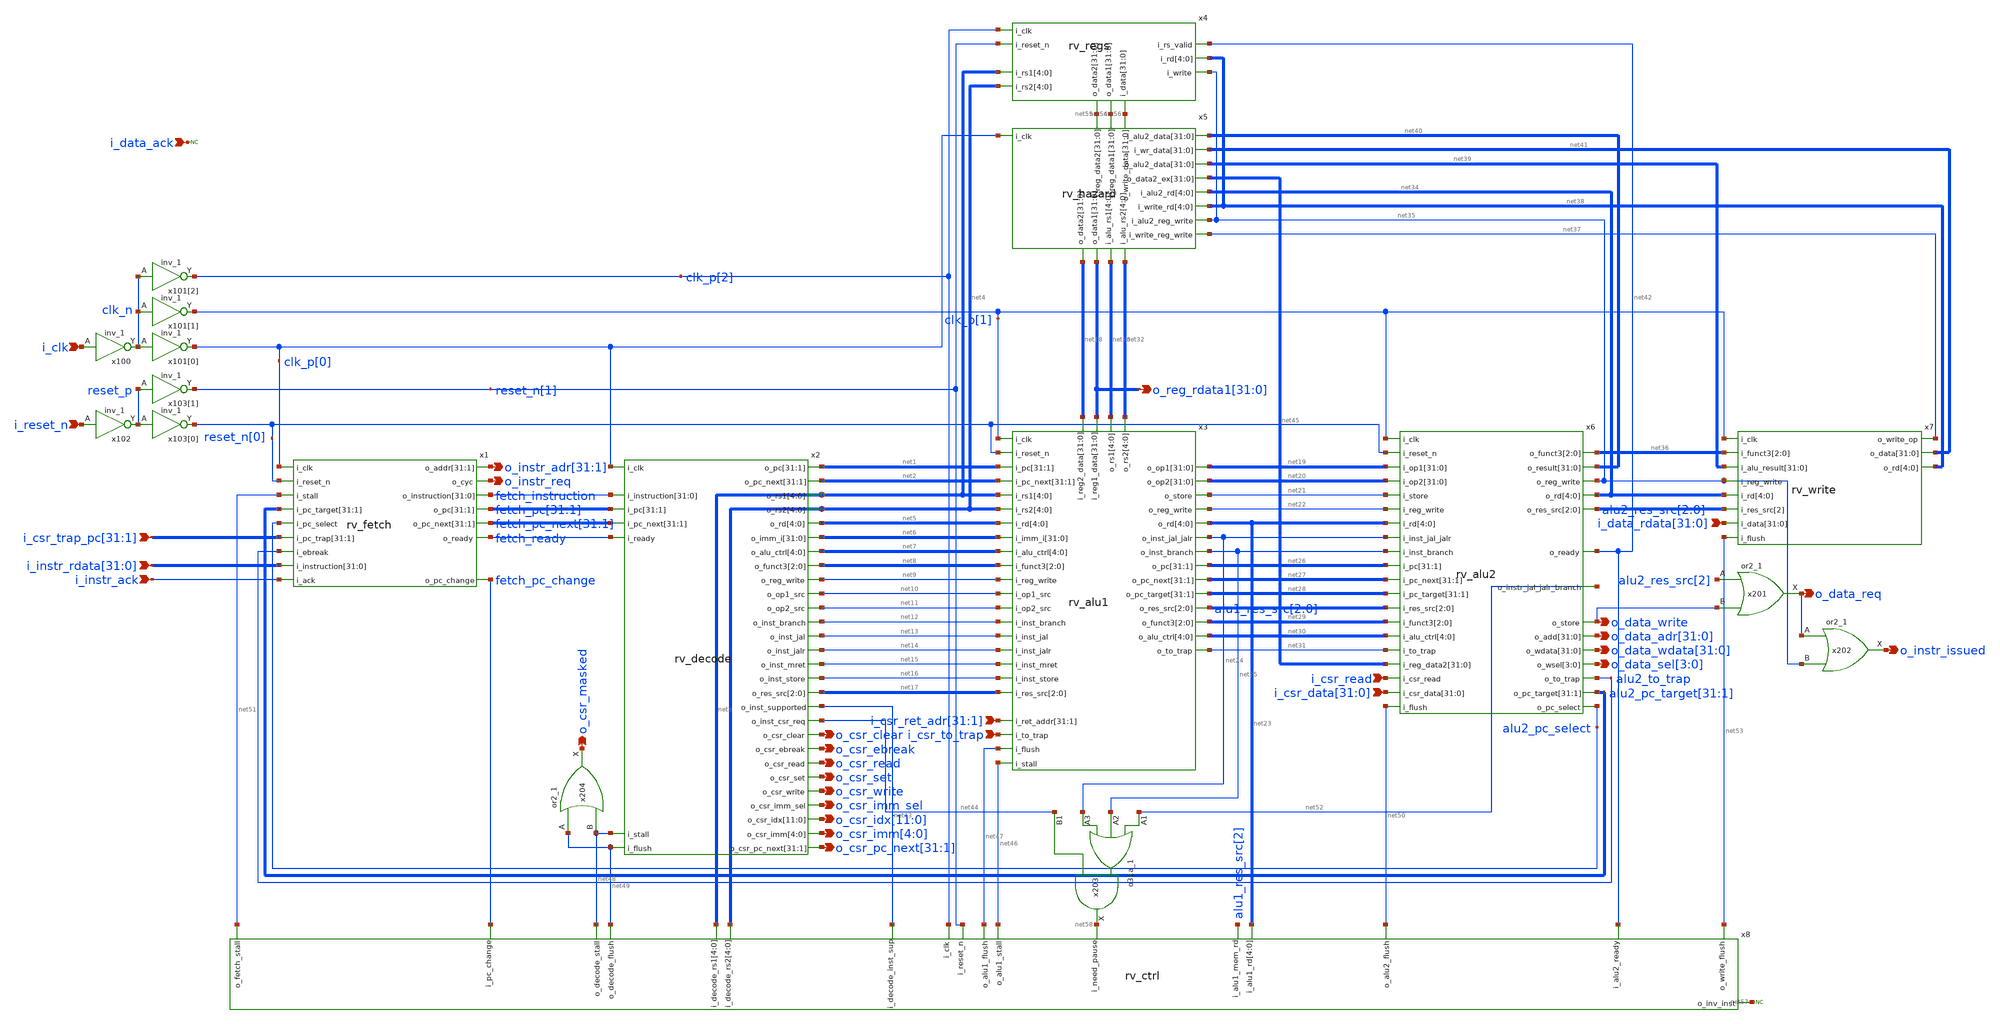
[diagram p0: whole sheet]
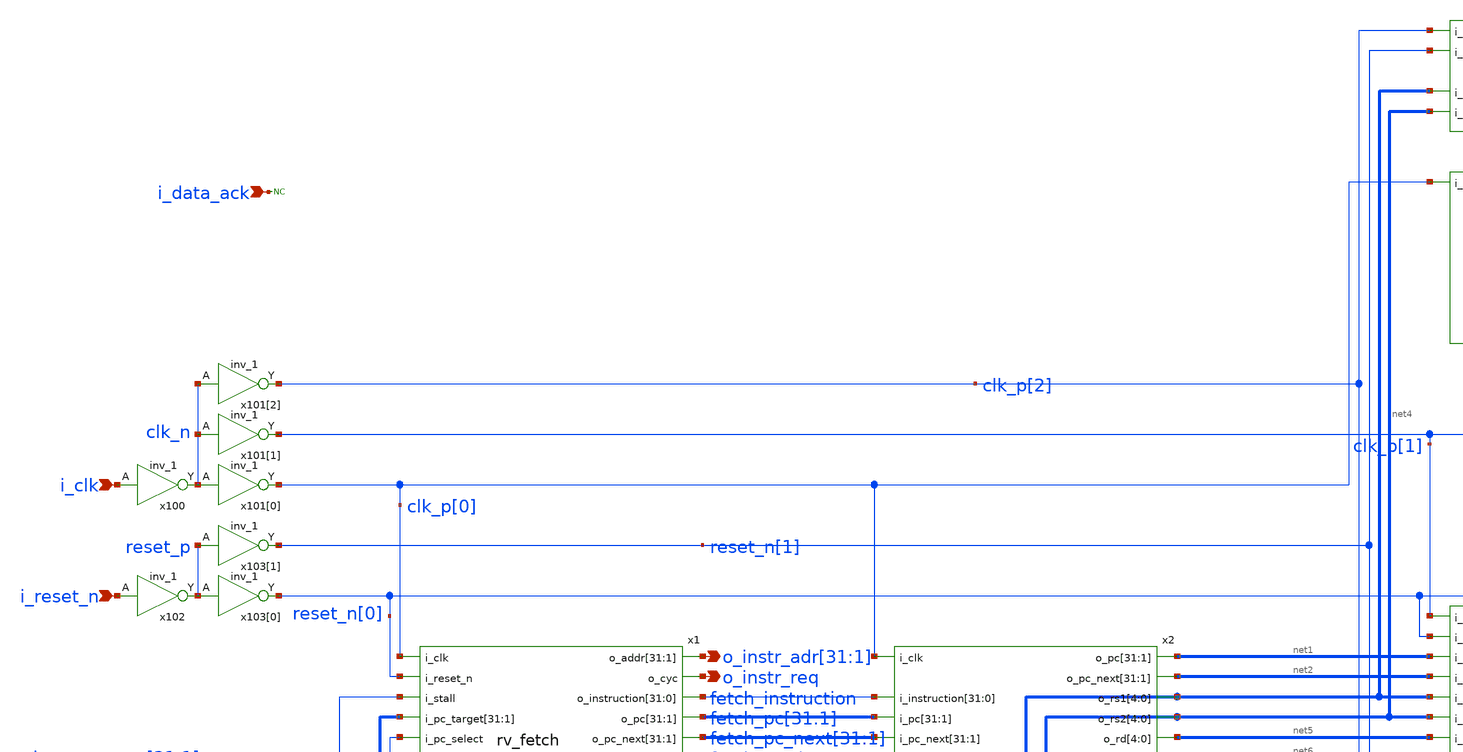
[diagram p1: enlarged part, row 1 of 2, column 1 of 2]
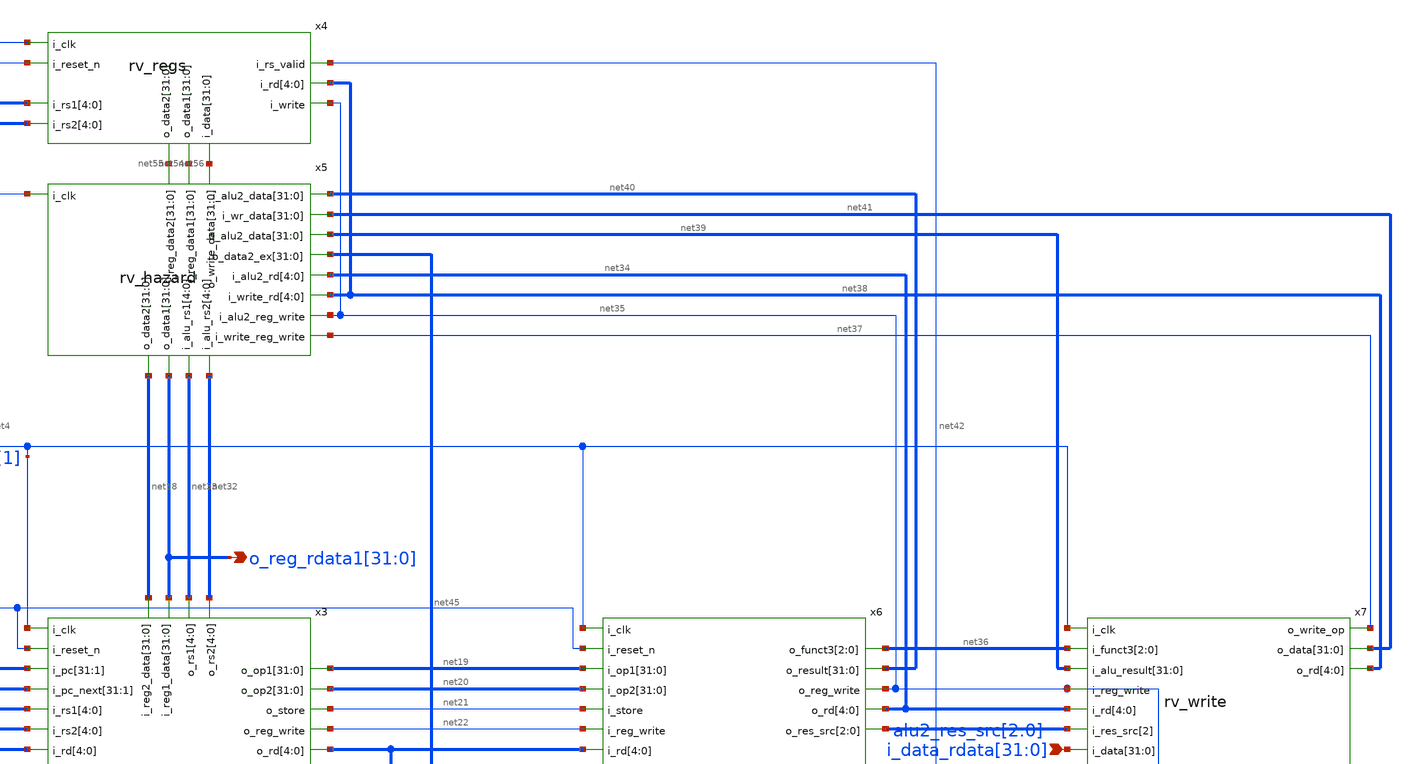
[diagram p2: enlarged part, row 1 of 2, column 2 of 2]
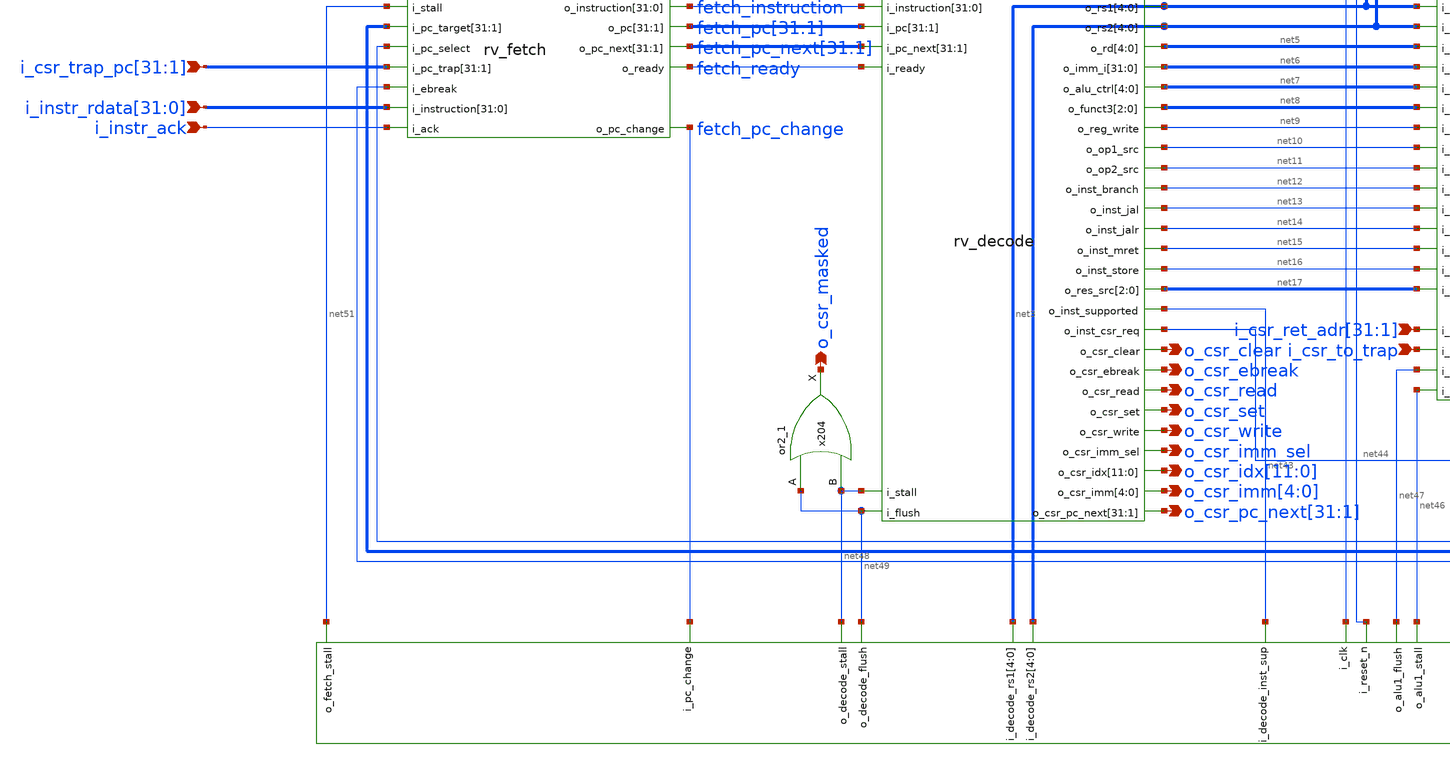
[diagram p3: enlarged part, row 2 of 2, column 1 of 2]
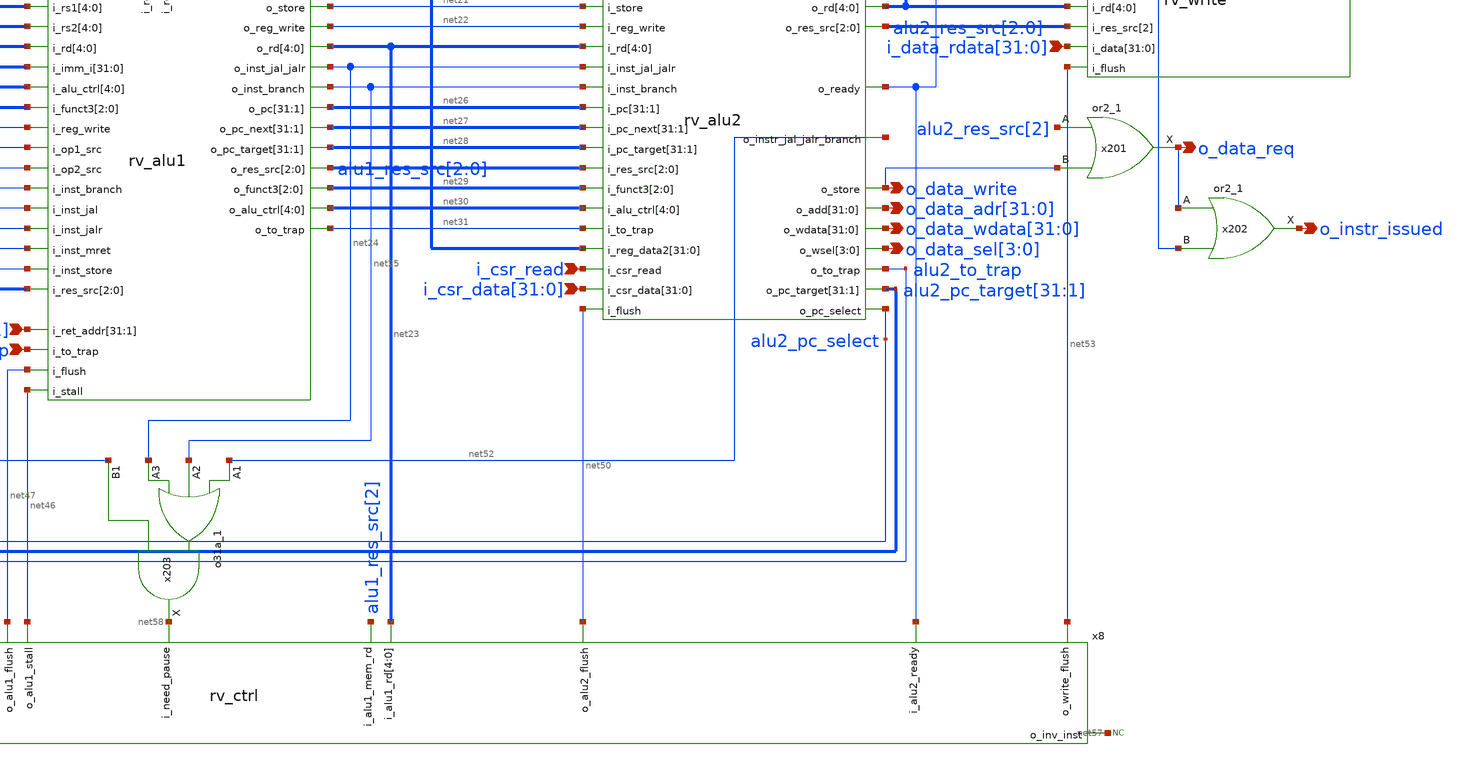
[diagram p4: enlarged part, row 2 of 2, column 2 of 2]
** sch_path: blocks/rv_core/rv_core.sch
**.subckt rv_core i_clk i_reset_n i_csr_read o_csr_clear o_data_req
*+ o_data_wdata[31],o_data_wdata[30],o_data_wdata[29],o_data_wdata[28],o_data_wdata[27],o_data_wdata[26],o_data_wdata[25],o_data_wdata[24],o_data_wdata[23],o_data_wdata[22],o_data_wdata[21],o_data_wdata[20],o_data_wdata[19],o_data_wdata[18],o_data_wdata[17],o_data_wdata[16],o_data_wdata[15],o_data_wdata[14],o_data_wdata[13],o_data_wdata[12],o_data_wdata[11],o_data_wdata[10],o_data_wdata[9],o_data_wdata[8],o_data_wdata[7],o_data_wdata[6],o_data_wdata[5],o_data_wdata[4],o_data_wdata[3],o_data_wdata[2],o_data_wdata[1],o_data_wdata[0] o_instr_issued
*+ o_data_adr[31],o_data_adr[30],o_data_adr[29],o_data_adr[28],o_data_adr[27],o_data_adr[26],o_data_adr[25],o_data_adr[24],o_data_adr[23],o_data_adr[22],o_data_adr[21],o_data_adr[20],o_data_adr[19],o_data_adr[18],o_data_adr[17],o_data_adr[16],o_data_adr[15],o_data_adr[14],o_data_adr[13],o_data_adr[12],o_data_adr[11],o_data_adr[10],o_data_adr[9],o_data_adr[8],o_data_adr[7],o_data_adr[6],o_data_adr[5],o_data_adr[4],o_data_adr[3],o_data_adr[2],o_data_adr[1],o_data_adr[0] o_data_sel[3],o_data_sel[2],o_data_sel[1],o_data_sel[0]
*+ i_csr_data[31],i_csr_data[30],i_csr_data[29],i_csr_data[28],i_csr_data[27],i_csr_data[26],i_csr_data[25],i_csr_data[24],i_csr_data[23],i_csr_data[22],i_csr_data[21],i_csr_data[20],i_csr_data[19],i_csr_data[18],i_csr_data[17],i_csr_data[16],i_csr_data[15],i_csr_data[14],i_csr_data[13],i_csr_data[12],i_csr_data[11],i_csr_data[10],i_csr_data[9],i_csr_data[8],i_csr_data[7],i_csr_data[6],i_csr_data[5],i_csr_data[4],i_csr_data[3],i_csr_data[2],i_csr_data[1],i_csr_data[0] i_csr_to_trap o_csr_ebreak o_csr_read o_csr_set o_csr_write o_csr_imm_sel
*+ i_csr_ret_adr[31],i_csr_ret_adr[30],i_csr_ret_adr[29],i_csr_ret_adr[28],i_csr_ret_adr[27],i_csr_ret_adr[26],i_csr_ret_adr[25],i_csr_ret_adr[24],i_csr_ret_adr[23],i_csr_ret_adr[22],i_csr_ret_adr[21],i_csr_ret_adr[20],i_csr_ret_adr[19],i_csr_ret_adr[18],i_csr_ret_adr[17],i_csr_ret_adr[16],i_csr_ret_adr[15],i_csr_ret_adr[14],i_csr_ret_adr[13],i_csr_ret_adr[12],i_csr_ret_adr[11],i_csr_ret_adr[10],i_csr_ret_adr[9],i_csr_ret_adr[8],i_csr_ret_adr[7],i_csr_ret_adr[6],i_csr_ret_adr[5],i_csr_ret_adr[4],i_csr_ret_adr[3],i_csr_ret_adr[2],i_csr_ret_adr[1]
*+ i_csr_trap_pc[31],i_csr_trap_pc[30],i_csr_trap_pc[29],i_csr_trap_pc[28],i_csr_trap_pc[27],i_csr_trap_pc[26],i_csr_trap_pc[25],i_csr_trap_pc[24],i_csr_trap_pc[23],i_csr_trap_pc[22],i_csr_trap_pc[21],i_csr_trap_pc[20],i_csr_trap_pc[19],i_csr_trap_pc[18],i_csr_trap_pc[17],i_csr_trap_pc[16],i_csr_trap_pc[15],i_csr_trap_pc[14],i_csr_trap_pc[13],i_csr_trap_pc[12],i_csr_trap_pc[11],i_csr_trap_pc[10],i_csr_trap_pc[9],i_csr_trap_pc[8],i_csr_trap_pc[7],i_csr_trap_pc[6],i_csr_trap_pc[5],i_csr_trap_pc[4],i_csr_trap_pc[3],i_csr_trap_pc[2],i_csr_trap_pc[1]
*+ o_csr_idx[11],o_csr_idx[10],o_csr_idx[9],o_csr_idx[8],o_csr_idx[7],o_csr_idx[6],o_csr_idx[5],o_csr_idx[4],o_csr_idx[3],o_csr_idx[2],o_csr_idx[1],o_csr_idx[0] o_csr_imm[4],o_csr_imm[3],o_csr_imm[2],o_csr_imm[1],o_csr_imm[0]
*+ o_csr_pc_next[31],o_csr_pc_next[30],o_csr_pc_next[29],o_csr_pc_next[28],o_csr_pc_next[27],o_csr_pc_next[26],o_csr_pc_next[25],o_csr_pc_next[24],o_csr_pc_next[23],o_csr_pc_next[22],o_csr_pc_next[21],o_csr_pc_next[20],o_csr_pc_next[19],o_csr_pc_next[18],o_csr_pc_next[17],o_csr_pc_next[16],o_csr_pc_next[15],o_csr_pc_next[14],o_csr_pc_next[13],o_csr_pc_next[12],o_csr_pc_next[11],o_csr_pc_next[10],o_csr_pc_next[9],o_csr_pc_next[8],o_csr_pc_next[7],o_csr_pc_next[6],o_csr_pc_next[5],o_csr_pc_next[4],o_csr_pc_next[3],o_csr_pc_next[2],o_csr_pc_next[1]
*+ o_reg_rdata1[31],o_reg_rdata1[30],o_reg_rdata1[29],o_reg_rdata1[28],o_reg_rdata1[27],o_reg_rdata1[26],o_reg_rdata1[25],o_reg_rdata1[24],o_reg_rdata1[23],o_reg_rdata1[22],o_reg_rdata1[21],o_reg_rdata1[20],o_reg_rdata1[19],o_reg_rdata1[18],o_reg_rdata1[17],o_reg_rdata1[16],o_reg_rdata1[15],o_reg_rdata1[14],o_reg_rdata1[13],o_reg_rdata1[12],o_reg_rdata1[11],o_reg_rdata1[10],o_reg_rdata1[9],o_reg_rdata1[8],o_reg_rdata1[7],o_reg_rdata1[6],o_reg_rdata1[5],o_reg_rdata1[4],o_reg_rdata1[3],o_reg_rdata1[2],o_reg_rdata1[1],o_reg_rdata1[0] i_data_ack o_data_write
*+ i_data_rdata[31],i_data_rdata[30],i_data_rdata[29],i_data_rdata[28],i_data_rdata[27],i_data_rdata[26],i_data_rdata[25],i_data_rdata[24],i_data_rdata[23],i_data_rdata[22],i_data_rdata[21],i_data_rdata[20],i_data_rdata[19],i_data_rdata[18],i_data_rdata[17],i_data_rdata[16],i_data_rdata[15],i_data_rdata[14],i_data_rdata[13],i_data_rdata[12],i_data_rdata[11],i_data_rdata[10],i_data_rdata[9],i_data_rdata[8],i_data_rdata[7],i_data_rdata[6],i_data_rdata[5],i_data_rdata[4],i_data_rdata[3],i_data_rdata[2],i_data_rdata[1],i_data_rdata[0] i_instr_ack o_instr_req
*+ i_instr_rdata[31],i_instr_rdata[30],i_instr_rdata[29],i_instr_rdata[28],i_instr_rdata[27],i_instr_rdata[26],i_instr_rdata[25],i_instr_rdata[24],i_instr_rdata[23],i_instr_rdata[22],i_instr_rdata[21],i_instr_rdata[20],i_instr_rdata[19],i_instr_rdata[18],i_instr_rdata[17],i_instr_rdata[16],i_instr_rdata[15],i_instr_rdata[14],i_instr_rdata[13],i_instr_rdata[12],i_instr_rdata[11],i_instr_rdata[10],i_instr_rdata[9],i_instr_rdata[8],i_instr_rdata[7],i_instr_rdata[6],i_instr_rdata[5],i_instr_rdata[4],i_instr_rdata[3],i_instr_rdata[2],i_instr_rdata[1],i_instr_rdata[0]
*+ o_instr_adr[31],o_instr_adr[30],o_instr_adr[29],o_instr_adr[28],o_instr_adr[27],o_instr_adr[26],o_instr_adr[25],o_instr_adr[24],o_instr_adr[23],o_instr_adr[22],o_instr_adr[21],o_instr_adr[20],o_instr_adr[19],o_instr_adr[18],o_instr_adr[17],o_instr_adr[16],o_instr_adr[15],o_instr_adr[14],o_instr_adr[13],o_instr_adr[12],o_instr_adr[11],o_instr_adr[10],o_instr_adr[9],o_instr_adr[8],o_instr_adr[7],o_instr_adr[6],o_instr_adr[5],o_instr_adr[4],o_instr_adr[3],o_instr_adr[2],o_instr_adr[1] o_csr_masked
*.ipin i_clk
*.ipin i_reset_n
*.ipin i_csr_read
*.opin o_csr_clear
*.opin o_data_req
*.opin
*+ o_data_wdata[31],o_data_wdata[30],o_data_wdata[29],o_data_wdata[28],o_data_wdata[27],o_data_wdata[26],o_data_wdata[25],o_data_wdata[24],o_data_wdata[23],o_data_wdata[22],o_data_wdata[21],o_data_wdata[20],o_data_wdata[19],o_data_wdata[18],o_data_wdata[17],o_data_wdata[16],o_data_wdata[15],o_data_wdata[14],o_data_wdata[13],o_data_wdata[12],o_data_wdata[11],o_data_wdata[10],o_data_wdata[9],o_data_wdata[8],o_data_wdata[7],o_data_wdata[6],o_data_wdata[5],o_data_wdata[4],o_data_wdata[3],o_data_wdata[2],o_data_wdata[1],o_data_wdata[0]
*.opin o_instr_issued
*.opin
*+ o_data_adr[31],o_data_adr[30],o_data_adr[29],o_data_adr[28],o_data_adr[27],o_data_adr[26],o_data_adr[25],o_data_adr[24],o_data_adr[23],o_data_adr[22],o_data_adr[21],o_data_adr[20],o_data_adr[19],o_data_adr[18],o_data_adr[17],o_data_adr[16],o_data_adr[15],o_data_adr[14],o_data_adr[13],o_data_adr[12],o_data_adr[11],o_data_adr[10],o_data_adr[9],o_data_adr[8],o_data_adr[7],o_data_adr[6],o_data_adr[5],o_data_adr[4],o_data_adr[3],o_data_adr[2],o_data_adr[1],o_data_adr[0]
*.opin o_data_sel[3],o_data_sel[2],o_data_sel[1],o_data_sel[0]
*.ipin
*+ i_csr_data[31],i_csr_data[30],i_csr_data[29],i_csr_data[28],i_csr_data[27],i_csr_data[26],i_csr_data[25],i_csr_data[24],i_csr_data[23],i_csr_data[22],i_csr_data[21],i_csr_data[20],i_csr_data[19],i_csr_data[18],i_csr_data[17],i_csr_data[16],i_csr_data[15],i_csr_data[14],i_csr_data[13],i_csr_data[12],i_csr_data[11],i_csr_data[10],i_csr_data[9],i_csr_data[8],i_csr_data[7],i_csr_data[6],i_csr_data[5],i_csr_data[4],i_csr_data[3],i_csr_data[2],i_csr_data[1],i_csr_data[0]
*.ipin i_csr_to_trap
*.opin o_csr_ebreak
*.opin o_csr_read
*.opin o_csr_set
*.opin o_csr_write
*.opin o_csr_imm_sel
*.ipin
*+ i_csr_ret_adr[31],i_csr_ret_adr[30],i_csr_ret_adr[29],i_csr_ret_adr[28],i_csr_ret_adr[27],i_csr_ret_adr[26],i_csr_ret_adr[25],i_csr_ret_adr[24],i_csr_ret_adr[23],i_csr_ret_adr[22],i_csr_ret_adr[21],i_csr_ret_adr[20],i_csr_ret_adr[19],i_csr_ret_adr[18],i_csr_ret_adr[17],i_csr_ret_adr[16],i_csr_ret_adr[15],i_csr_ret_adr[14],i_csr_ret_adr[13],i_csr_ret_adr[12],i_csr_ret_adr[11],i_csr_ret_adr[10],i_csr_ret_adr[9],i_csr_ret_adr[8],i_csr_ret_adr[7],i_csr_ret_adr[6],i_csr_ret_adr[5],i_csr_ret_adr[4],i_csr_ret_adr[3],i_csr_ret_adr[2],i_csr_ret_adr[1]
*.ipin
*+ i_csr_trap_pc[31],i_csr_trap_pc[30],i_csr_trap_pc[29],i_csr_trap_pc[28],i_csr_trap_pc[27],i_csr_trap_pc[26],i_csr_trap_pc[25],i_csr_trap_pc[24],i_csr_trap_pc[23],i_csr_trap_pc[22],i_csr_trap_pc[21],i_csr_trap_pc[20],i_csr_trap_pc[19],i_csr_trap_pc[18],i_csr_trap_pc[17],i_csr_trap_pc[16],i_csr_trap_pc[15],i_csr_trap_pc[14],i_csr_trap_pc[13],i_csr_trap_pc[12],i_csr_trap_pc[11],i_csr_trap_pc[10],i_csr_trap_pc[9],i_csr_trap_pc[8],i_csr_trap_pc[7],i_csr_trap_pc[6],i_csr_trap_pc[5],i_csr_trap_pc[4],i_csr_trap_pc[3],i_csr_trap_pc[2],i_csr_trap_pc[1]
*.opin
*+ o_csr_idx[11],o_csr_idx[10],o_csr_idx[9],o_csr_idx[8],o_csr_idx[7],o_csr_idx[6],o_csr_idx[5],o_csr_idx[4],o_csr_idx[3],o_csr_idx[2],o_csr_idx[1],o_csr_idx[0]
*.opin o_csr_imm[4],o_csr_imm[3],o_csr_imm[2],o_csr_imm[1],o_csr_imm[0]
*.opin
*+ o_csr_pc_next[31],o_csr_pc_next[30],o_csr_pc_next[29],o_csr_pc_next[28],o_csr_pc_next[27],o_csr_pc_next[26],o_csr_pc_next[25],o_csr_pc_next[24],o_csr_pc_next[23],o_csr_pc_next[22],o_csr_pc_next[21],o_csr_pc_next[20],o_csr_pc_next[19],o_csr_pc_next[18],o_csr_pc_next[17],o_csr_pc_next[16],o_csr_pc_next[15],o_csr_pc_next[14],o_csr_pc_next[13],o_csr_pc_next[12],o_csr_pc_next[11],o_csr_pc_next[10],o_csr_pc_next[9],o_csr_pc_next[8],o_csr_pc_next[7],o_csr_pc_next[6],o_csr_pc_next[5],o_csr_pc_next[4],o_csr_pc_next[3],o_csr_pc_next[2],o_csr_pc_next[1]
*.opin
*+ o_reg_rdata1[31],o_reg_rdata1[30],o_reg_rdata1[29],o_reg_rdata1[28],o_reg_rdata1[27],o_reg_rdata1[26],o_reg_rdata1[25],o_reg_rdata1[24],o_reg_rdata1[23],o_reg_rdata1[22],o_reg_rdata1[21],o_reg_rdata1[20],o_reg_rdata1[19],o_reg_rdata1[18],o_reg_rdata1[17],o_reg_rdata1[16],o_reg_rdata1[15],o_reg_rdata1[14],o_reg_rdata1[13],o_reg_rdata1[12],o_reg_rdata1[11],o_reg_rdata1[10],o_reg_rdata1[9],o_reg_rdata1[8],o_reg_rdata1[7],o_reg_rdata1[6],o_reg_rdata1[5],o_reg_rdata1[4],o_reg_rdata1[3],o_reg_rdata1[2],o_reg_rdata1[1],o_reg_rdata1[0]
*.ipin i_data_ack
*.opin o_data_write
*.ipin
*+ i_data_rdata[31],i_data_rdata[30],i_data_rdata[29],i_data_rdata[28],i_data_rdata[27],i_data_rdata[26],i_data_rdata[25],i_data_rdata[24],i_data_rdata[23],i_data_rdata[22],i_data_rdata[21],i_data_rdata[20],i_data_rdata[19],i_data_rdata[18],i_data_rdata[17],i_data_rdata[16],i_data_rdata[15],i_data_rdata[14],i_data_rdata[13],i_data_rdata[12],i_data_rdata[11],i_data_rdata[10],i_data_rdata[9],i_data_rdata[8],i_data_rdata[7],i_data_rdata[6],i_data_rdata[5],i_data_rdata[4],i_data_rdata[3],i_data_rdata[2],i_data_rdata[1],i_data_rdata[0]
*.ipin i_instr_ack
*.opin o_instr_req
*.ipin
*+ i_instr_rdata[31],i_instr_rdata[30],i_instr_rdata[29],i_instr_rdata[28],i_instr_rdata[27],i_instr_rdata[26],i_instr_rdata[25],i_instr_rdata[24],i_instr_rdata[23],i_instr_rdata[22],i_instr_rdata[21],i_instr_rdata[20],i_instr_rdata[19],i_instr_rdata[18],i_instr_rdata[17],i_instr_rdata[16],i_instr_rdata[15],i_instr_rdata[14],i_instr_rdata[13],i_instr_rdata[12],i_instr_rdata[11],i_instr_rdata[10],i_instr_rdata[9],i_instr_rdata[8],i_instr_rdata[7],i_instr_rdata[6],i_instr_rdata[5],i_instr_rdata[4],i_instr_rdata[3],i_instr_rdata[2],i_instr_rdata[1],i_instr_rdata[0]
*.opin
*+ o_instr_adr[31],o_instr_adr[30],o_instr_adr[29],o_instr_adr[28],o_instr_adr[27],o_instr_adr[26],o_instr_adr[25],o_instr_adr[24],o_instr_adr[23],o_instr_adr[22],o_instr_adr[21],o_instr_adr[20],o_instr_adr[19],o_instr_adr[18],o_instr_adr[17],o_instr_adr[16],o_instr_adr[15],o_instr_adr[14],o_instr_adr[13],o_instr_adr[12],o_instr_adr[11],o_instr_adr[10],o_instr_adr[9],o_instr_adr[8],o_instr_adr[7],o_instr_adr[6],o_instr_adr[5],o_instr_adr[4],o_instr_adr[3],o_instr_adr[2],o_instr_adr[1]
*.opin o_csr_masked
x1 fetch_pc_change clk_p[0] reset_n[0] o_instr_adr[31] o_instr_adr[30] o_instr_adr[29]
+ o_instr_adr[28] o_instr_adr[27] o_instr_adr[26] o_instr_adr[25] o_instr_adr[24] o_instr_adr[23] o_instr_adr[22]
+ o_instr_adr[21] o_instr_adr[20] o_instr_adr[19] o_instr_adr[18] o_instr_adr[17] o_instr_adr[16] o_instr_adr[15]
+ o_instr_adr[14] o_instr_adr[13] o_instr_adr[12] o_instr_adr[11] o_instr_adr[10] o_instr_adr[9] o_instr_adr[8]
+ o_instr_adr[7] o_instr_adr[6] o_instr_adr[5] o_instr_adr[4] o_instr_adr[3] o_instr_adr[2] o_instr_adr[1]
+ o_instr_req net51 fetch_instruction fetch_instruction fetch_instruction fetch_instruction fetch_instruction
+ fetch_instruction fetch_instruction fetch_instruction fetch_instruction fetch_instruction fetch_instruction
+ fetch_instruction fetch_instruction fetch_instruction fetch_instruction fetch_instruction fetch_instruction
+ fetch_instruction fetch_instruction fetch_instruction fetch_instruction fetch_instruction fetch_instruction
+ fetch_instruction fetch_instruction fetch_instruction fetch_instruction fetch_instruction fetch_instruction
+ fetch_instruction fetch_instruction fetch_instruction alu2_pc_target[31] alu2_pc_target[30] alu2_pc_target[29]
+ alu2_pc_target[28] alu2_pc_target[27] alu2_pc_target[26] alu2_pc_target[25] alu2_pc_target[24] alu2_pc_target[23]
+ alu2_pc_target[22] alu2_pc_target[21] alu2_pc_target[20] alu2_pc_target[19] alu2_pc_target[18] alu2_pc_target[17]
+ alu2_pc_target[16] alu2_pc_target[15] alu2_pc_target[14] alu2_pc_target[13] alu2_pc_target[12] alu2_pc_target[11]
+ alu2_pc_target[10] alu2_pc_target[9] alu2_pc_target[8] alu2_pc_target[7] alu2_pc_target[6] alu2_pc_target[5]
+ alu2_pc_target[4] alu2_pc_target[3] alu2_pc_target[2] alu2_pc_target[1] alu2_pc_select fetch_pc[31] fetch_pc[30]
+ fetch_pc[29] fetch_pc[28] fetch_pc[27] fetch_pc[26] fetch_pc[25] fetch_pc[24] fetch_pc[23] fetch_pc[22]
+ fetch_pc[21] fetch_pc[20] fetch_pc[19] fetch_pc[18] fetch_pc[17] fetch_pc[16] fetch_pc[15] fetch_pc[14]
+ fetch_pc[13] fetch_pc[12] fetch_pc[11] fetch_pc[10] fetch_pc[9] fetch_pc[8] fetch_pc[7] fetch_pc[6] fetch_pc[5]
+ fetch_pc[4] fetch_pc[3] fetch_pc[2] fetch_pc[1] fetch_pc_next[31] fetch_pc_next[30] fetch_pc_next[29]
+ fetch_pc_next[28] fetch_pc_next[27] fetch_pc_next[26] fetch_pc_next[25] fetch_pc_next[24] fetch_pc_next[23]
+ fetch_pc_next[22] fetch_pc_next[21] fetch_pc_next[20] fetch_pc_next[19] fetch_pc_next[18] fetch_pc_next[17]
+ fetch_pc_next[16] fetch_pc_next[15] fetch_pc_next[14] fetch_pc_next[13] fetch_pc_next[12] fetch_pc_next[11]
+ fetch_pc_next[10] fetch_pc_next[9] fetch_pc_next[8] fetch_pc_next[7] fetch_pc_next[6] fetch_pc_next[5]
+ fetch_pc_next[4] fetch_pc_next[3] fetch_pc_next[2] fetch_pc_next[1] i_csr_trap_pc[31] i_csr_trap_pc[30]
+ i_csr_trap_pc[29] i_csr_trap_pc[28] i_csr_trap_pc[27] i_csr_trap_pc[26] i_csr_trap_pc[25] i_csr_trap_pc[24]
+ i_csr_trap_pc[23] i_csr_trap_pc[22] i_csr_trap_pc[21] i_csr_trap_pc[20] i_csr_trap_pc[19] i_csr_trap_pc[18]
+ i_csr_trap_pc[17] i_csr_trap_pc[16] i_csr_trap_pc[15] i_csr_trap_pc[14] i_csr_trap_pc[13] i_csr_trap_pc[12]
+ i_csr_trap_pc[11] i_csr_trap_pc[10] i_csr_trap_pc[9] i_csr_trap_pc[8] i_csr_trap_pc[7] i_csr_trap_pc[6]
+ i_csr_trap_pc[5] i_csr_trap_pc[4] i_csr_trap_pc[3] i_csr_trap_pc[2] i_csr_trap_pc[1] fetch_ready alu2_to_trap
+ i_instr_rdata[31] i_instr_rdata[30] i_instr_rdata[29] i_instr_rdata[28] i_instr_rdata[27] i_instr_rdata[26]
+ i_instr_rdata[25] i_instr_rdata[24] i_instr_rdata[23] i_instr_rdata[22] i_instr_rdata[21] i_instr_rdata[20]
+ i_instr_rdata[19] i_instr_rdata[18] i_instr_rdata[17] i_instr_rdata[16] i_instr_rdata[15] i_instr_rdata[14]
+ i_instr_rdata[13] i_instr_rdata[12] i_instr_rdata[11] i_instr_rdata[10] i_instr_rdata[9] i_instr_rdata[8]
+ i_instr_rdata[7] i_instr_rdata[6] i_instr_rdata[5] i_instr_rdata[4] i_instr_rdata[3] i_instr_rdata[2]
+ i_instr_rdata[1] i_instr_rdata[0] i_instr_ack rv_fetch
x100 i_clk VSS VSS VCC VCC clk_n sky130_fd_sc_hs__inv_1
x102 i_reset_n VSS VSS VCC VCC reset_p sky130_fd_sc_hs__inv_1
x103[0] reset_p VSS VSS VCC VCC reset_n[0] sky130_fd_sc_hs__inv_1
x101[2] clk_n VSS VSS VCC VCC clk_p[2] sky130_fd_sc_hs__inv_1
x101[1] clk_n VSS VSS VCC VCC clk_p[1] sky130_fd_sc_hs__inv_1
x101[0] clk_n VSS VSS VCC VCC clk_p[0] sky130_fd_sc_hs__inv_1
x103[1] reset_p VSS VSS VCC VCC reset_n[1] sky130_fd_sc_hs__inv_1
x2 net1[30] net1[29] net1[28] net1[27] net1[26] net1[25] net1[24] net1[23] net1[22] net1[21]
+ net1[20] net1[19] net1[18] net1[17] net1[16] net1[15] net1[14] net1[13] net1[12] net1[11] net1[10] net1[9]
+ net1[8] net1[7] net1[6] net1[5] net1[4] net1[3] net1[2] net1[1] net1[0] clk_p[0] net48 net2[30] net2[29]
+ net2[28] net2[27] net2[26] net2[25] net2[24] net2[23] net2[22] net2[21] net2[20] net2[19] net2[18] net2[17]
+ net2[16] net2[15] net2[14] net2[13] net2[12] net2[11] net2[10] net2[9] net2[8] net2[7] net2[6] net2[5]
+ net2[4] net2[3] net2[2] net2[1] net2[0] net49 net3[4] net3[3] net3[2] net3[1] net3[0] fetch_instruction
+ fetch_instruction fetch_instruction fetch_instruction fetch_instruction fetch_instruction fetch_instruction
+ fetch_instruction fetch_instruction fetch_instruction fetch_instruction fetch_instruction fetch_instruction
+ fetch_instruction fetch_instruction fetch_instruction fetch_instruction fetch_instruction fetch_instruction
+ fetch_instruction fetch_instruction fetch_instruction fetch_instruction fetch_instruction fetch_instruction
+ fetch_instruction fetch_instruction fetch_instruction fetch_instruction fetch_instruction fetch_instruction
+ fetch_instruction net4[4] net4[3] net4[2] net4[1] net4[0] net5[4] net5[3] net5[2] net5[1] net5[0] fetch_pc[31]
+ fetch_pc[30] fetch_pc[29] fetch_pc[28] fetch_pc[27] fetch_pc[26] fetch_pc[25] fetch_pc[24] fetch_pc[23]
+ fetch_pc[22] fetch_pc[21] fetch_pc[20] fetch_pc[19] fetch_pc[18] fetch_pc[17] fetch_pc[16] fetch_pc[15]
+ fetch_pc[14] fetch_pc[13] fetch_pc[12] fetch_pc[11] fetch_pc[10] fetch_pc[9] fetch_pc[8] fetch_pc[7] fetch_pc[6]
+ fetch_pc[5] fetch_pc[4] fetch_pc[3] fetch_pc[2] fetch_pc[1] net6[31] net6[30] net6[29] net6[28] net6[27]
+ net6[26] net6[25] net6[24] net6[23] net6[22] net6[21] net6[20] net6[19] net6[18] net6[17] net6[16] net6[15]
+ net6[14] net6[13] net6[12] net6[11] net6[10] net6[9] net6[8] net6[7] net6[6] net6[5] net6[4] net6[3] net6[2]
+ net6[1] net6[0] fetch_pc_next[31] fetch_pc_next[30] fetch_pc_next[29] fetch_pc_next[28] fetch_pc_next[27]
+ fetch_pc_next[26] fetch_pc_next[25] fetch_pc_next[24] fetch_pc_next[23] fetch_pc_next[22] fetch_pc_next[21]
+ fetch_pc_next[20] fetch_pc_next[19] fetch_pc_next[18] fetch_pc_next[17] fetch_pc_next[16] fetch_pc_next[15]
+ fetch_pc_next[14] fetch_pc_next[13] fetch_pc_next[12] fetch_pc_next[11] fetch_pc_next[10] fetch_pc_next[9]
+ fetch_pc_next[8] fetch_pc_next[7] fetch_pc_next[6] fetch_pc_next[5] fetch_pc_next[4] fetch_pc_next[3]
+ fetch_pc_next[2] fetch_pc_next[1] fetch_ready net7[4] net7[3] net7[2] net7[1] net7[0] net8[2] net8[1] net8[0] net9
+ net10 net11 net12 net44 net13 net14 net15 net16 net43 net17[2] net17[1] net17[0] o_csr_clear o_csr_ebreak
+ o_csr_read o_csr_set o_csr_write o_csr_imm_sel o_csr_idx[11] o_csr_idx[10] o_csr_idx[9] o_csr_idx[8]
+ o_csr_idx[7] o_csr_idx[6] o_csr_idx[5] o_csr_idx[4] o_csr_idx[3] o_csr_idx[2] o_csr_idx[1] o_csr_idx[0]
+ o_csr_imm[4] o_csr_imm[3] o_csr_imm[2] o_csr_imm[1] o_csr_imm[0] o_csr_pc_next[31] o_csr_pc_next[30]
+ o_csr_pc_next[29] o_csr_pc_next[28] o_csr_pc_next[27] o_csr_pc_next[26] o_csr_pc_next[25] o_csr_pc_next[24]
+ o_csr_pc_next[23] o_csr_pc_next[22] o_csr_pc_next[21] o_csr_pc_next[20] o_csr_pc_next[19] o_csr_pc_next[18]
+ o_csr_pc_next[17] o_csr_pc_next[16] o_csr_pc_next[15] o_csr_pc_next[14] o_csr_pc_next[13] o_csr_pc_next[12]
+ o_csr_pc_next[11] o_csr_pc_next[10] o_csr_pc_next[9] o_csr_pc_next[8] o_csr_pc_next[7] o_csr_pc_next[6]
+ o_csr_pc_next[5] o_csr_pc_next[4] o_csr_pc_next[3] o_csr_pc_next[2] o_csr_pc_next[1] rv_decode
x3 clk_p[1] net19[31] net19[30] net19[29] net19[28] net19[27] net19[26] net19[25] net19[24]
+ net19[23] net19[22] net19[21] net19[20] net19[19] net19[18] net19[17] net19[16] net19[15] net19[14] net19[13]
+ net19[12] net19[11] net19[10] net19[9] net19[8] net19[7] net19[6] net19[5] net19[4] net19[3] net19[2]
+ net19[1] net19[0] reset_n[0] net20[31] net20[30] net20[29] net20[28] net20[27] net20[26] net20[25] net20[24]
+ net20[23] net20[22] net20[21] net20[20] net20[19] net20[18] net20[17] net20[16] net20[15] net20[14] net20[13]
+ net20[12] net20[11] net20[10] net20[9] net20[8] net20[7] net20[6] net20[5] net20[4] net20[3] net20[2]
+ net20[1] net20[0] net1[30] net1[29] net1[28] net1[27] net1[26] net1[25] net1[24] net1[23] net1[22] net1[21]
+ net1[20] net1[19] net1[18] net1[17] net1[16] net1[15] net1[14] net1[13] net1[12] net1[11] net1[10] net1[9]
+ net1[8] net1[7] net1[6] net1[5] net1[4] net1[3] net1[2] net1[1] net1[0] net21 net22 net2[30] net2[29]
+ net2[28] net2[27] net2[26] net2[25] net2[24] net2[23] net2[22] net2[21] net2[20] net2[19] net2[18] net2[17]
+ net2[16] net2[15] net2[14] net2[13] net2[12] net2[11] net2[10] net2[9] net2[8] net2[7] net2[6] net2[5]
+ net2[4] net2[3] net2[2] net2[1] net2[0] net33[4] net33[3] net33[2] net33[1] net33[0] net3[4] net3[3]
+ net3[2] net3[1] net3[0] net4[4] net4[3] net4[2] net4[1] net4[0] net32[4] net32[3] net32[2] net32[1]
+ net32[0] net5[4] net5[3] net5[2] net5[1] net5[0] net23[4] net23[3] net23[2] net23[1] net23[0] net6[31]
+ net6[30] net6[29] net6[28] net6[27] net6[26] net6[25] net6[24] net6[23] net6[22] net6[21] net6[20] net6[19]
+ net6[18] net6[17] net6[16] net6[15] net6[14] net6[13] net6[12] net6[11] net6[10] net6[9] net6[8] net6[7]
+ net6[6] net6[5] net6[4] net6[3] net6[2] net6[1] net6[0] net24 net7[4] net7[3] net7[2] net7[1] net7[0] net25
+ net8[2] net8[1] net8[0] net26[30] net26[29] net26[28] net26[27] net26[26] net26[25] net26[24] net26[23]
+ net26[22] net26[21] net26[20] net26[19] net26[18] net26[17] net26[16] net26[15] net26[14] net26[13] net26[12]
+ net26[11] net26[10] net26[9] net26[8] net26[7] net26[6] net26[5] net26[4] net26[3] net26[2] net26[1] net26[0]
+ net27[30] net27[29] net27[28] net27[27] net27[26] net27[25] net27[24] net27[23] net27[22] net27[21] net27[20]
+ net27[19] net27[18] net27[17] net27[16] net27[15] net27[14] net27[13] net27[12] net27[11] net27[10] net27[9]
+ net27[8] net27[7] net27[6] net27[5] net27[4] net27[3] net27[2] net27[1] net27[0] net9 net28[30] net28[29]
+ net28[28] net28[27] net28[26] net28[25] net28[24] net28[23] net28[22] net28[21] net28[20] net28[19] net28[18]
+ net28[17] net28[16] net28[15] net28[14] net28[13] net28[12] net28[11] net28[10] net28[9] net28[8] net28[7]
+ net28[6] net28[5] net28[4] net28[3] net28[2] net28[1] net28[0] net10 net11 alu1_res_src[2] alu1_res_src[1]
+ alu1_res_src[0] net12 net29[2] net29[1] net29[0] net30[4] net30[3] net30[2] net30[1] net30[0] net13 net31 net14
+ net15 net16 net17[2] net17[1] net17[0] o_reg_rdata1[31] o_reg_rdata1[30] o_reg_rdata1[29]
+ o_reg_rdata1[28] o_reg_rdata1[27] o_reg_rdata1[26] o_reg_rdata1[25] o_reg_rdata1[24] o_reg_rdata1[23]
+ o_reg_rdata1[22] o_reg_rdata1[21] o_reg_rdata1[20] o_reg_rdata1[19] o_reg_rdata1[18] o_reg_rdata1[17]
+ o_reg_rdata1[16] o_reg_rdata1[15] o_reg_rdata1[14] o_reg_rdata1[13] o_reg_rdata1[12] o_reg_rdata1[11]
+ o_reg_rdata1[10] o_reg_rdata1[9] o_reg_rdata1[8] o_reg_rdata1[7] o_reg_rdata1[6] o_reg_rdata1[5] o_reg_rdata1[4]
+ o_reg_rdata1[3] o_reg_rdata1[2] o_reg_rdata1[1] o_reg_rdata1[0] net18[31] net18[30] net18[29] net18[28] net18[27]
+ net18[26] net18[25] net18[24] net18[23] net18[22] net18[21] net18[20] net18[19] net18[18] net18[17] net18[16]
+ net18[15] net18[14] net18[13] net18[12] net18[11] net18[10] net18[9] net18[8] net18[7] net18[6] net18[5]
+ net18[4] net18[3] net18[2] net18[1] net18[0] i_csr_to_trap net47 net46 i_csr_ret_adr[31] i_csr_ret_adr[30]
+ i_csr_ret_adr[29] i_csr_ret_adr[28] i_csr_ret_adr[27] i_csr_ret_adr[26] i_csr_ret_adr[25] i_csr_ret_adr[24]
+ i_csr_ret_adr[23] i_csr_ret_adr[22] i_csr_ret_adr[21] i_csr_ret_adr[20] i_csr_ret_adr[19] i_csr_ret_adr[18]
+ i_csr_ret_adr[17] i_csr_ret_adr[16] i_csr_ret_adr[15] i_csr_ret_adr[14] i_csr_ret_adr[13] i_csr_ret_adr[12]
+ i_csr_ret_adr[11] i_csr_ret_adr[10] i_csr_ret_adr[9] i_csr_ret_adr[8] i_csr_ret_adr[7] i_csr_ret_adr[6]
+ i_csr_ret_adr[5] i_csr_ret_adr[4] i_csr_ret_adr[3] i_csr_ret_adr[2] i_csr_ret_adr[1] rv_alu1
x4 net54[31] net54[30] net54[29] net54[28] net54[27] net54[26] net54[25] net54[24] net54[23]
+ net54[22] net54[21] net54[20] net54[19] net54[18] net54[17] net54[16] net54[15] net54[14] net54[13] net54[12]
+ net54[11] net54[10] net54[9] net54[8] net54[7] net54[6] net54[5] net54[4] net54[3] net54[2] net54[1] net54[0]
+ clk_p[2] reset_n[1] net55[31] net55[30] net55[29] net55[28] net55[27] net55[26] net55[25] net55[24]
+ net55[23] net55[22] net55[21] net55[20] net55[19] net55[18] net55[17] net55[16] net55[15] net55[14] net55[13]
+ net55[12] net55[11] net55[10] net55[9] net55[8] net55[7] net55[6] net55[5] net55[4] net55[3] net55[2]
+ net55[1] net55[0] net42 net35 net3[4] net3[3] net3[2] net3[1] net3[0] net4[4] net4[3] net4[2] net4[1]
+ net4[0] net38[4] net38[3] net38[2] net38[1] net38[0] net56[31] net56[30] net56[29] net56[28] net56[27]
+ net56[26] net56[25] net56[24] net56[23] net56[22] net56[21] net56[20] net56[19] net56[18] net56[17] net56[16]
+ net56[15] net56[14] net56[13] net56[12] net56[11] net56[10] net56[9] net56[8] net56[7] net56[6] net56[5]
+ net56[4] net56[3] net56[2] net56[1] net56[0] rv_regs
x5 clk_p[0] o_reg_rdata1[31] o_reg_rdata1[30] o_reg_rdata1[29] o_reg_rdata1[28] o_reg_rdata1[27]
+ o_reg_rdata1[26] o_reg_rdata1[25] o_reg_rdata1[24] o_reg_rdata1[23] o_reg_rdata1[22] o_reg_rdata1[21]
+ o_reg_rdata1[20] o_reg_rdata1[19] o_reg_rdata1[18] o_reg_rdata1[17] o_reg_rdata1[16] o_reg_rdata1[15]
+ o_reg_rdata1[14] o_reg_rdata1[13] o_reg_rdata1[12] o_reg_rdata1[11] o_reg_rdata1[10] o_reg_rdata1[9] o_reg_rdata1[8]
+ o_reg_rdata1[7] o_reg_rdata1[6] o_reg_rdata1[5] o_reg_rdata1[4] o_reg_rdata1[3] o_reg_rdata1[2] o_reg_rdata1[1]
+ o_reg_rdata1[0] net33[4] net33[3] net33[2] net33[1] net33[0] net18[31] net18[30] net18[29] net18[28] net18[27]
+ net18[26] net18[25] net18[24] net18[23] net18[22] net18[21] net18[20] net18[19] net18[18] net18[17] net18[16]
+ net18[15] net18[14] net18[13] net18[12] net18[11] net18[10] net18[9] net18[8] net18[7] net18[6] net18[5]
+ net18[4] net18[3] net18[2] net18[1] net18[0] net32[4] net32[3] net32[2] net32[1] net32[0] net39[31]
+ net39[30] net39[29] net39[28] net39[27] net39[26] net39[25] net39[24] net39[23] net39[22] net39[21] net39[20]
+ net39[19] net39[18] net39[17] net39[16] net39[15] net39[14] net39[13] net39[12] net39[11] net39[10] net39[9]
+ net39[8] net39[7] net39[6] net39[5] net39[4] net39[3] net39[2] net39[1] net39[0] net34[4] net34[3] net34[2]
+ net34[1] net34[0] net56[31] net56[30] net56[29] net56[28] net56[27] net56[26] net56[25] net56[24] net56[23]
+ net56[22] net56[21] net56[20] net56[19] net56[18] net56[17] net56[16] net56[15] net56[14] net56[13] net56[12]
+ net56[11] net56[10] net56[9] net56[8] net56[7] net56[6] net56[5] net56[4] net56[3] net56[2] net56[1] net56[0]
+ net38[4] net38[3] net38[2] net38[1] net38[0] net45[31] net45[30] net45[29] net45[28] net45[27] net45[26]
+ net45[25] net45[24] net45[23] net45[22] net45[21] net45[20] net45[19] net45[18] net45[17] net45[16] net45[15]
+ net45[14] net45[13] net45[12] net45[11] net45[10] net45[9] net45[8] net45[7] net45[6] net45[5] net45[4]
+ net45[3] net45[2] net45[1] net45[0] net35 net37 net54[31] net54[30] net54[29] net54[28] net54[27] net54[26]
+ net54[25] net54[24] net54[23] net54[22] net54[21] net54[20] net54[19] net54[18] net54[17] net54[16] net54[15]
+ net54[14] net54[13] net54[12] net54[11] net54[10] net54[9] net54[8] net54[7] net54[6] net54[5] net54[4]
+ net54[3] net54[2] net54[1] net54[0] net55[31] net55[30] net55[29] net55[28] net55[27] net55[26] net55[25]
+ net55[24] net55[23] net55[22] net55[21] net55[20] net55[19] net55[18] net55[17] net55[16] net55[15] net55[14]
+ net55[13] net55[12] net55[11] net55[10] net55[9] net55[8] net55[7] net55[6] net55[5] net55[4] net55[3]
+ net55[2] net55[1] net55[0] net40[31] net40[30] net40[29] net40[28] net40[27] net40[26] net40[25] net40[24]
+ net40[23] net40[22] net40[21] net40[20] net40[19] net40[18] net40[17] net40[16] net40[15] net40[14] net40[13]
+ net40[12] net40[11] net40[10] net40[9] net40[8] net40[7] net40[6] net40[5] net40[4] net40[3] net40[2]
+ net40[1] net40[0] net41[31] net41[30] net41[29] net41[28] net41[27] net41[26] net41[25] net41[24] net41[23]
+ net41[22] net41[21] net41[20] net41[19] net41[18] net41[17] net41[16] net41[15] net41[14] net41[13] net41[12]
+ net41[11] net41[10] net41[9] net41[8] net41[7] net41[6] net41[5] net41[4] net41[3] net41[2] net41[1] net41[0]
+ rv_hazard
x6 alu2_pc_select clk_p[1] reset_n[0] net40[31] net40[30] net40[29] net40[28] net40[27] net40[26]
+ net40[25] net40[24] net40[23] net40[22] net40[21] net40[20] net40[19] net40[18] net40[17] net40[16] net40[15]
+ net40[14] net40[13] net40[12] net40[11] net40[10] net40[9] net40[8] net40[7] net40[6] net40[5] net40[4]
+ net40[3] net40[2] net40[1] net40[0] net19[31] net19[30] net19[29] net19[28] net19[27] net19[26] net19[25]
+ net19[24] net19[23] net19[22] net19[21] net19[20] net19[19] net19[18] net19[17] net19[16] net19[15] net19[14]
+ net19[13] net19[12] net19[11] net19[10] net19[9] net19[8] net19[7] net19[6] net19[5] net19[4] net19[3]
+ net19[2] net19[1] net19[0] o_data_adr[31] o_data_adr[30] o_data_adr[29] o_data_adr[28] o_data_adr[27]
+ o_data_adr[26] o_data_adr[25] o_data_adr[24] o_data_adr[23] o_data_adr[22] o_data_adr[21] o_data_adr[20]
+ o_data_adr[19] o_data_adr[18] o_data_adr[17] o_data_adr[16] o_data_adr[15] o_data_adr[14] o_data_adr[13]
+ o_data_adr[12] o_data_adr[11] o_data_adr[10] o_data_adr[9] o_data_adr[8] o_data_adr[7] o_data_adr[6] o_data_adr[5]
+ o_data_adr[4] o_data_adr[3] o_data_adr[2] o_data_adr[1] o_data_adr[0] o_data_write net20[31] net20[30] net20[29]
+ net20[28] net20[27] net20[26] net20[25] net20[24] net20[23] net20[22] net20[21] net20[20] net20[19] net20[18]
+ net20[17] net20[16] net20[15] net20[14] net20[13] net20[12] net20[11] net20[10] net20[9] net20[8] net20[7]
+ net20[6] net20[5] net20[4] net20[3] net20[2] net20[1] net20[0] net35 net21 net34[4] net34[3] net34[2]
+ net34[1] net34[0] net22 net23[4] net23[3] net23[2] net23[1] net23[0] alu2_pc_target[31] alu2_pc_target[30]
+ alu2_pc_target[29] alu2_pc_target[28] alu2_pc_target[27] alu2_pc_target[26] alu2_pc_target[25] alu2_pc_target[24]
+ alu2_pc_target[23] alu2_pc_target[22] alu2_pc_target[21] alu2_pc_target[20] alu2_pc_target[19] alu2_pc_target[18]
+ alu2_pc_target[17] alu2_pc_target[16] alu2_pc_target[15] alu2_pc_target[14] alu2_pc_target[13] alu2_pc_target[12]
+ alu2_pc_target[11] alu2_pc_target[10] alu2_pc_target[9] alu2_pc_target[8] alu2_pc_target[7] alu2_pc_target[6]
+ alu2_pc_target[5] alu2_pc_target[4] alu2_pc_target[3] alu2_pc_target[2] alu2_pc_target[1] alu2_res_src[2]
+ alu2_res_src[1] alu2_res_src[0] net24 net25 o_data_wdata[31] o_data_wdata[30] o_data_wdata[29] o_data_wdata[28]
+ o_data_wdata[27] o_data_wdata[26] o_data_wdata[25] o_data_wdata[24] o_data_wdata[23] o_data_wdata[22]
+ o_data_wdata[21] o_data_wdata[20] o_data_wdata[19] o_data_wdata[18] o_data_wdata[17] o_data_wdata[16]
+ o_data_wdata[15] o_data_wdata[14] o_data_wdata[13] o_data_wdata[12] o_data_wdata[11] o_data_wdata[10]
+ o_data_wdata[9] o_data_wdata[8] o_data_wdata[7] o_data_wdata[6] o_data_wdata[5] o_data_wdata[4] o_data_wdata[3]
+ o_data_wdata[2] o_data_wdata[1] o_data_wdata[0] o_data_sel[3] o_data_sel[2] o_data_sel[1] o_data_sel[0] net26[30]
+ net26[29] net26[28] net26[27] net26[26] net26[25] net26[24] net26[23] net26[22] net26[21] net26[20] net26[19]
+ net26[18] net26[17] net26[16] net26[15] net26[14] net26[13] net26[12] net26[11] net26[10] net26[9] net26[8]
+ net26[7] net26[6] net26[5] net26[4] net26[3] net26[2] net26[1] net26[0] net27[30] net27[29] net27[28]
+ net27[27] net27[26] net27[25] net27[24] net27[23] net27[22] net27[21] net27[20] net27[19] net27[18] net27[17]
+ net27[16] net27[15] net27[14] net27[13] net27[12] net27[11] net27[10] net27[9] net27[8] net27[7] net27[6]
+ net27[5] net27[4] net27[3] net27[2] net27[1] net27[0] net36[2] net36[1] net36[0] alu2_to_trap net28[30]
+ net28[29] net28[28] net28[27] net28[26] net28[25] net28[24] net28[23] net28[22] net28[21] net28[20] net28[19]
+ net28[18] net28[17] net28[16] net28[15] net28[14] net28[13] net28[12] net28[11] net28[10] net28[9] net28[8]
+ net28[7] net28[6] net28[5] net28[4] net28[3] net28[2] net28[1] net28[0] alu1_res_src[2] alu1_res_src[1]
+ alu1_res_src[0] net42 net29[2] net29[1] net29[0] net30[4] net30[3] net30[2] net30[1] net30[0] net31 net45[31]
+ net45[30] net45[29] net45[28] net45[27] net45[26] net45[25] net45[24] net45[23] net45[22] net45[21] net45[20]
+ net45[19] net45[18] net45[17] net45[16] net45[15] net45[14] net45[13] net45[12] net45[11] net45[10] net45[9]
+ net45[8] net45[7] net45[6] net45[5] net45[4] net45[3] net45[2] net45[1] net45[0] i_csr_read i_csr_data[31]
+ i_csr_data[30] i_csr_data[29] i_csr_data[28] i_csr_data[27] i_csr_data[26] i_csr_data[25] i_csr_data[24]
+ i_csr_data[23] i_csr_data[22] i_csr_data[21] i_csr_data[20] i_csr_data[19] i_csr_data[18] i_csr_data[17]
+ i_csr_data[16] i_csr_data[15] i_csr_data[14] i_csr_data[13] i_csr_data[12] i_csr_data[11] i_csr_data[10]
+ i_csr_data[9] i_csr_data[8] i_csr_data[7] i_csr_data[6] i_csr_data[5] i_csr_data[4] i_csr_data[3] i_csr_data[2]
+ i_csr_data[1] i_csr_data[0] net50 net52 rv_alu2
x7 clk_p[1] net37 net36[2] net36[1] net36[0] net41[31] net41[30] net41[29] net41[28] net41[27]
+ net41[26] net41[25] net41[24] net41[23] net41[22] net41[21] net41[20] net41[19] net41[18] net41[17] net41[16]
+ net41[15] net41[14] net41[13] net41[12] net41[11] net41[10] net41[9] net41[8] net41[7] net41[6] net41[5]
+ net41[4] net41[3] net41[2] net41[1] net41[0] net39[31] net39[30] net39[29] net39[28] net39[27] net39[26]
+ net39[25] net39[24] net39[23] net39[22] net39[21] net39[20] net39[19] net39[18] net39[17] net39[16] net39[15]
+ net39[14] net39[13] net39[12] net39[11] net39[10] net39[9] net39[8] net39[7] net39[6] net39[5] net39[4]
+ net39[3] net39[2] net39[1] net39[0] net38[4] net38[3] net38[2] net38[1] net38[0] net35 net34[4] net34[3]
+ net34[2] net34[1] net34[0] alu2_res_src[2] i_data_rdata[31] i_data_rdata[30] i_data_rdata[29]
+ i_data_rdata[28] i_data_rdata[27] i_data_rdata[26] i_data_rdata[25] i_data_rdata[24] i_data_rdata[23]
+ i_data_rdata[22] i_data_rdata[21] i_data_rdata[20] i_data_rdata[19] i_data_rdata[18] i_data_rdata[17]
+ i_data_rdata[16] i_data_rdata[15] i_data_rdata[14] i_data_rdata[13] i_data_rdata[12] i_data_rdata[11]
+ i_data_rdata[10] i_data_rdata[9] i_data_rdata[8] i_data_rdata[7] i_data_rdata[6] i_data_rdata[5] i_data_rdata[4]
+ i_data_rdata[3] i_data_rdata[2] i_data_rdata[1] i_data_rdata[0] net53 rv_write
x201 alu2_res_src[2] o_data_write VSS VSS VCC VCC o_data_req sky130_fd_sc_hs__or2_1
x202 o_data_req net35 VSS VSS VCC VCC o_instr_issued sky130_fd_sc_hs__or2_1
* noconn i_data_ack
x8 clk_p[2] net51 reset_n[1] net49 net48 fetch_pc_change net47 net43 net46 net42 alu1_res_src[2]
+ net50 net57 net58 net3[4] net3[3] net3[2] net3[1] net3[0] net4[4] net4[3] net4[2] net4[1] net4[0]
+ net23[4] net23[3] net23[2] net23[1] net23[0] net53 rv_ctrl
x203 net52 net25 net24 net44 VSS VSS VCC VCC net58 sky130_fd_sc_hs__o31a_1
* noconn #net57
x204 net49 net48 VSS VSS VCC VCC o_csr_masked sky130_fd_sc_hs__or2_1
**.ends
.end
